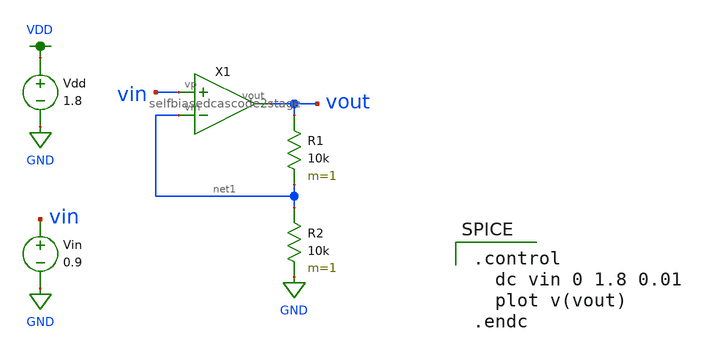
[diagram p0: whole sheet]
** sch_path: Final DAC files/schematics/opamp/selfbiasedcascode2stage_test.sch
**.subckt selfbiasedcascode2stage_test
Vdd VDD GND 1.8
X1 vin net1 vout selfbiasedcascode2stage
Vin vin GND 0.9
R1 vout net1 10k m=1
R2 net1 GND 10k m=1
**** begin user architecture code

.option wnflag=1
.param MC_SWITCH=0.0
.lib ~/skywater/skywater-pdk/libraries/sky130_fd_pr_ngspice/latest/models/sky130.lib.spice tt


.control
  dc vin 0 1.8 0.01
  plot v(vout)
.endc

**** end user architecture code
**.ends

* expanding   symbol:  /home/madvlsi/Documents/selfbiasedcascode/selfbiasedcascode2stage.sym # of
*+ pins=3
** sym_path: Final DAC files/schematics/opamp/selfbiasedcascode2stage.sym
** sch_path: Final DAC files/schematics/opamp/selfbiasedcascode2stage.sch
.subckt selfbiasedcascode2stage vp vm vout
*.ipin vp
*.ipin vm
*.opin vout
XM1 net11 net1 GND GND sky130_fd_pr__nfet_01v8 L=0.6 W=3 nf=1 ad='int((nf+1)/2) * W/nf * 0.29' as='int((nf+2)/2) * W/nf * 0.29'
+ pd='2*int((nf+1)/2) * (W/nf + 0.29)' ps='2*int((nf+2)/2) * (W/nf + 0.29)' nrd='0.29 / W' nrs='0.29 / W'
+ sa=0 sb=0 sd=0 mult=1 m=1
XM9 net12 net3 VDD VDD sky130_fd_pr__pfet_01v8 L=0.6 W=3 nf=1 ad='int((nf+1)/2) * W/nf * 0.29' as='int((nf+2)/2) * W/nf * 0.29'
+ pd='2*int((nf+1)/2) * (W/nf + 0.29)' ps='2*int((nf+2)/2) * (W/nf + 0.29)' nrd='0.29 / W' nrs='0.29 / W'
+ sa=0 sb=0 sd=0 mult=1 m=1
XM2 net5 net1 GND GND sky130_fd_pr__nfet_01v8 L=0.6 W=3 nf=1 ad='int((nf+1)/2) * W/nf * 0.29' as='int((nf+2)/2) * W/nf * 0.29'
+ pd='2*int((nf+1)/2) * (W/nf + 0.29)' ps='2*int((nf+2)/2) * (W/nf + 0.29)' nrd='0.29 / W' nrs='0.29 / W'
+ sa=0 sb=0 sd=0 mult=1 m=1
XM3 net6 net2 net11 GND sky130_fd_pr__nfet_01v8 L=0.6 W=3 nf=1 ad='int((nf+1)/2) * W/nf * 0.29' as='int((nf+2)/2) * W/nf * 0.29'
+ pd='2*int((nf+1)/2) * (W/nf + 0.29)' ps='2*int((nf+2)/2) * (W/nf + 0.29)' nrd='0.29 / W' nrs='0.29 / W'
+ sa=0 sb=0 sd=0 mult=1 m=1
XM4 net2 net2 net5 GND sky130_fd_pr__nfet_01v8 L=0.6 W=3 nf=1 ad='int((nf+1)/2) * W/nf * 0.29' as='int((nf+2)/2) * W/nf * 0.29'
+ pd='2*int((nf+1)/2) * (W/nf + 0.29)' ps='2*int((nf+2)/2) * (W/nf + 0.29)' nrd='0.29 / W' nrs='0.29 / W'
+ sa=0 sb=0 sd=0 mult=1 m=1
XM5 net1 net1 net5 GND sky130_fd_pr__nfet_01v8 L=0.6 W=3 nf=1 ad='int((nf+1)/2) * W/nf * 0.29' as='int((nf+2)/2) * W/nf * 0.29'
+ pd='2*int((nf+1)/2) * (W/nf + 0.29)' ps='2*int((nf+2)/2) * (W/nf + 0.29)' nrd='0.29 / W' nrs='0.29 / W'
+ sa=0 sb=0 sd=0 mult=1 m=1
XM6 net10 net1 GND GND sky130_fd_pr__nfet_01v8 L=0.6 W=3 nf=1 ad='int((nf+1)/2) * W/nf * 0.29' as='int((nf+2)/2) * W/nf * 0.29'
+ pd='2*int((nf+1)/2) * (W/nf + 0.29)' ps='2*int((nf+2)/2) * (W/nf + 0.29)' nrd='0.29 / W' nrs='0.29 / W'
+ sa=0 sb=0 sd=0 mult=1 m=1
XM7 net12 vp net10 GND sky130_fd_pr__nfet_01v8 L=0.6 W=3 nf=1 ad='int((nf+1)/2) * W/nf * 0.29' as='int((nf+2)/2) * W/nf * 0.29'
+ pd='2*int((nf+1)/2) * (W/nf + 0.29)' ps='2*int((nf+2)/2) * (W/nf + 0.29)' nrd='0.29 / W' nrs='0.29 / W'
+ sa=0 sb=0 sd=0 mult=1 m=1
XM8 net4 vm net10 GND sky130_fd_pr__nfet_01v8 L=0.6 W=3 nf=1 ad='int((nf+1)/2) * W/nf * 0.29' as='int((nf+2)/2) * W/nf * 0.29'
+ pd='2*int((nf+1)/2) * (W/nf + 0.29)' ps='2*int((nf+2)/2) * (W/nf + 0.29)' nrd='0.29 / W' nrs='0.29 / W'
+ sa=0 sb=0 sd=0 mult=1 m=1
XM10 net4 net3 VDD VDD sky130_fd_pr__pfet_01v8 L=0.6 W=3 nf=1 ad='int((nf+1)/2) * W/nf * 0.29' as='int((nf+2)/2) * W/nf * 0.29'
+ pd='2*int((nf+1)/2) * (W/nf + 0.29)' ps='2*int((nf+2)/2) * (W/nf + 0.29)' nrd='0.29 / W' nrs='0.29 / W'
+ sa=0 sb=0 sd=0 mult=1 m=1
XM11 net6 net2 net12 VDD sky130_fd_pr__pfet_01v8 L=0.6 W=3 nf=1 ad='int((nf+1)/2) * W/nf * 0.29' as='int((nf+2)/2) * W/nf * 0.29'
+ pd='2*int((nf+1)/2) * (W/nf + 0.29)' ps='2*int((nf+2)/2) * (W/nf + 0.29)' nrd='0.29 / W' nrs='0.29 / W'
+ sa=0 sb=0 sd=0 mult=1 m=1
XM12 net2 net2 net4 VDD sky130_fd_pr__pfet_01v8 L=0.6 W=3 nf=1 ad='int((nf+1)/2) * W/nf * 0.29' as='int((nf+2)/2) * W/nf * 0.29'
+ pd='2*int((nf+1)/2) * (W/nf + 0.29)' ps='2*int((nf+2)/2) * (W/nf + 0.29)' nrd='0.29 / W' nrs='0.29 / W'
+ sa=0 sb=0 sd=0 mult=1 m=1
XM13 net3 net3 net4 VDD sky130_fd_pr__pfet_01v8 L=0.6 W=3 nf=1 ad='int((nf+1)/2) * W/nf * 0.29' as='int((nf+2)/2) * W/nf * 0.29'
+ pd='2*int((nf+1)/2) * (W/nf + 0.29)' ps='2*int((nf+2)/2) * (W/nf + 0.29)' nrd='0.29 / W' nrs='0.29 / W'
+ sa=0 sb=0 sd=0 mult=1 m=1
XM14 net7 net3 VDD VDD sky130_fd_pr__pfet_01v8 L=0.6 W=3 nf=1 ad='int((nf+1)/2) * W/nf * 0.29' as='int((nf+2)/2) * W/nf * 0.29'
+ pd='2*int((nf+1)/2) * (W/nf + 0.29)' ps='2*int((nf+2)/2) * (W/nf + 0.29)' nrd='0.29 / W' nrs='0.29 / W'
+ sa=0 sb=0 sd=0 mult=1 m=1
XM15 net5 vm net7 VDD sky130_fd_pr__pfet_01v8 L=0.6 W=3 nf=1 ad='int((nf+1)/2) * W/nf * 0.29' as='int((nf+2)/2) * W/nf * 0.29'
+ pd='2*int((nf+1)/2) * (W/nf + 0.29)' ps='2*int((nf+2)/2) * (W/nf + 0.29)' nrd='0.29 / W' nrs='0.29 / W'
+ sa=0 sb=0 sd=0 mult=1 m=1
XM16 net11 vp net7 VDD sky130_fd_pr__pfet_01v8 L=0.6 W=3 nf=1 ad='int((nf+1)/2) * W/nf * 0.29' as='int((nf+2)/2) * W/nf * 0.29'
+ pd='2*int((nf+1)/2) * (W/nf + 0.29)' ps='2*int((nf+2)/2) * (W/nf + 0.29)' nrd='0.29 / W' nrs='0.29 / W'
+ sa=0 sb=0 sd=0 mult=1 m=1
XM17 net8 net1 GND GND sky130_fd_pr__nfet_01v8 L=0.6 W=3 nf=1 ad='int((nf+1)/2) * W/nf * 0.29' as='int((nf+2)/2) * W/nf * 0.29'
+ pd='2*int((nf+1)/2) * (W/nf + 0.29)' ps='2*int((nf+2)/2) * (W/nf + 0.29)' nrd='0.29 / W' nrs='0.29 / W'
+ sa=0 sb=0 sd=0 mult=1 m=1
XM18 net3 net1 net8 GND sky130_fd_pr__nfet_01v8 L=0.6 W=3 nf=1 ad='int((nf+1)/2) * W/nf * 0.29' as='int((nf+2)/2) * W/nf * 0.29'
+ pd='2*int((nf+1)/2) * (W/nf + 0.29)' ps='2*int((nf+2)/2) * (W/nf + 0.29)' nrd='0.29 / W' nrs='0.29 / W'
+ sa=0 sb=0 sd=0 mult=1 m=1
XM19 VDD net1 net8 GND sky130_fd_pr__nfet_01v8 L=0.6 W=3 nf=1 ad='int((nf+1)/2) * W/nf * 0.29' as='int((nf+2)/2) * W/nf * 0.29'
+ pd='2*int((nf+1)/2) * (W/nf + 0.29)' ps='2*int((nf+2)/2) * (W/nf + 0.29)' nrd='0.29 / W' nrs='0.29 / W'
+ sa=0 sb=0 sd=0 mult=3 m=3
XM20 net1 net3 net9 VDD sky130_fd_pr__pfet_01v8 L=0.6 W=3 nf=1 ad='int((nf+1)/2) * W/nf * 0.29' as='int((nf+2)/2) * W/nf * 0.29'
+ pd='2*int((nf+1)/2) * (W/nf + 0.29)' ps='2*int((nf+2)/2) * (W/nf + 0.29)' nrd='0.29 / W' nrs='0.29 / W'
+ sa=0 sb=0 sd=0 mult=1 m=1
XM21 net9 net3 VDD VDD sky130_fd_pr__pfet_01v8 L=0.6 W=3 nf=1 ad='int((nf+1)/2) * W/nf * 0.29' as='int((nf+2)/2) * W/nf * 0.29'
+ pd='2*int((nf+1)/2) * (W/nf + 0.29)' ps='2*int((nf+2)/2) * (W/nf + 0.29)' nrd='0.29 / W' nrs='0.29 / W'
+ sa=0 sb=0 sd=0 mult=1 m=1
XM22 GND net3 net9 VDD sky130_fd_pr__pfet_01v8 L=0.6 W=3 nf=1 ad='int((nf+1)/2) * W/nf * 0.29' as='int((nf+2)/2) * W/nf * 0.29'
+ pd='2*int((nf+1)/2) * (W/nf + 0.29)' ps='2*int((nf+2)/2) * (W/nf + 0.29)' nrd='0.29 / W' nrs='0.29 / W'
+ sa=0 sb=0 sd=0 mult=3 m=3
XM23 vout net6 VDD VDD sky130_fd_pr__pfet_01v8 L=0.15 W=12 nf=1 ad='int((nf+1)/2) * W/nf * 0.29' as='int((nf+2)/2) * W/nf * 0.29'
+ pd='2*int((nf+1)/2) * (W/nf + 0.29)' ps='2*int((nf+2)/2) * (W/nf + 0.29)' nrd='0.29 / W' nrs='0.29 / W'
+ sa=0 sb=0 sd=0 mult=1 m=1
XM24 vout net6 GND GND sky130_fd_pr__nfet_01v8 L=0.15 W=6 nf=1 ad='int((nf+1)/2) * W/nf * 0.29' as='int((nf+2)/2) * W/nf * 0.29'
+ pd='2*int((nf+1)/2) * (W/nf + 0.29)' ps='2*int((nf+2)/2) * (W/nf + 0.29)' nrd='0.29 / W' nrs='0.29 / W'
+ sa=0 sb=0 sd=0 mult=1 m=1
C1 net6 vout 500f m=1
.ends

.GLOBAL VDD
.GLOBAL GND
.end
